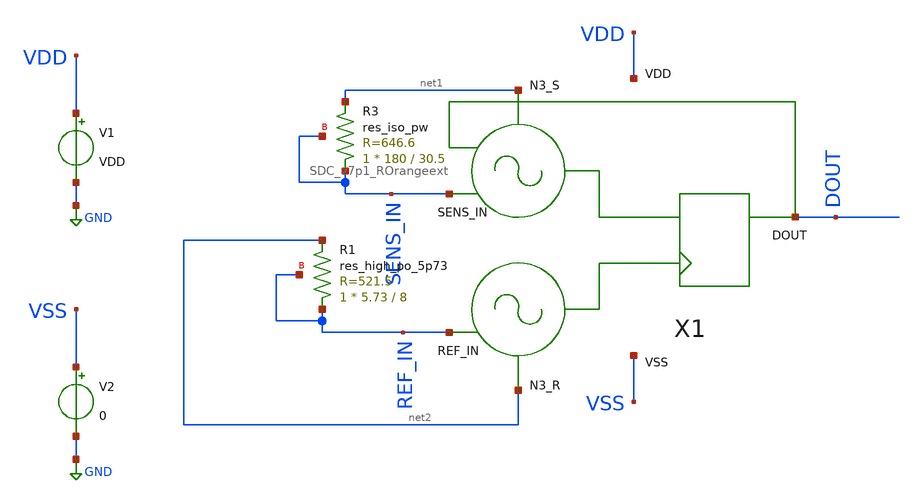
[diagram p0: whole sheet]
** sch_path: modules/SDC_v7p1_ROrangeext/test/test_SDCtsens_RINtsweep_9p1_ROrangeext.sch
**.subckt test_SDCtsens_RINtsweep_9p1_ROrangeext
V1 VDD GND VDD
V2 VSS GND 0
X1 SENS_IN REF_IN DOUT VDD VSS net1 net2 SDC_v7p1_ROrangeext
XR1 REF_IN net2 REF_IN sky130_fd_pr__res_high_po_5p73 L=8 mult=1 m=1
XR3 SENS_IN net1 SENS_IN sky130_fd_pr__res_iso_pw W=180 L=30.5 m=1
**** begin user architecture code

*.lib /home/jorge/Documents/Postdoc/share/pdk/sky130A/libs.tech/ngspice/sky130.lib.spice tt
.param VDD = 1.8
.ic v(SENS_IN) = 0
.ic v(REF_IN) = 1.8
.option temp = 0
.save v(DOUT)
.control
  run
*compose vin_var start=1.9p stop=2.11p step=0.02p
*compose vin_var start=8p stop=8.31p step=0.02p
*compose vin_var start=0.15p stop=0.15p step=0.02p
compose vin_var start=2.05k stop=2.05k step=0.02k
foreach val $&vin_var
  alter R_SENS $val
  tran 0.1n 20u
*  tran 0.1n 50u
end
*plot tran1.v(N2) tran2.v(N2) tran3.v(N2) tran4.v(N2) tran5.v(N2) tran6.v(N2) tran7.v(N2)
*+ tran8.v(N2) tran9.v(N2) tran10.v(N2) tran11.v(N2)
*wrdata ringosc_CINsweep_v2p1_Creal.txt tran1.v(N2) tran2.v(N2) tran3.v(N2) tran4.v(N2) tran5.v(N2)
*+ tran6.v(N2) tran7.v(N2) tran8.v(N2) tran9.v(N2) tran10.v(N2) tran11.v(N2)
*wrdata SDC_CINsweep_v5p7.txt tran1.v(DOUT) tran2.v(DOUT) tran3.v(DOUT) tran4.v(DOUT) tran5.v(DOUT)
*+ tran6.v(DOUT) tran7.v(DOUT) tran8.v(DOUT) tran9.v(DOUT) tran10.v(DOUT) tran11.v(DOUT) tran12.v(DOUT)
*+ tran13.v(DOUT) tran14.v(DOUT) tran15.v(DOUT) tran16.v(DOUT)
*wrdata SDC_RINsweep_v2p1_CLOAD.txt tran1.v(DOUT_CLOAD) tran2.v(DOUT_CLOAD) tran3.v(DOUT_CLOAD)
*+ tran4.v(DOUT_CLOAD) tran5.v(DOUT_CLOAD) tran6.v(DOUT_CLOAD) tran7.v(DOUT_CLOAD) tran8.v(DOUT_CLOAD) tran9.v(DOUT_CLOAD)
*+ tran10.v(DOUT_CLOAD) tran11.v(DOUT_CLOAD) tran12.v(DOUT_CLOAD) tran13.v(DOUT_CLOAD) tran14.v(DOUT_CLOAD)
*+ tran15.v(DOUT_CLOAD) tran16.v(DOUT_CLOAD)
*wrdata SDC_CINsweep_v5p7_CLOAD.txt tran1.v(DOUT_CLOAD)
wrdata SDC_RINsweep_v9p1_CLOAD_t0.txt tran1.v(DOUT)
.endc


** opencircuitdesign pdks install
.lib $::SKYWATER_MODELS/sky130.lib.spice tt


**** end user architecture code
**.ends
.GLOBAL GND
.end
